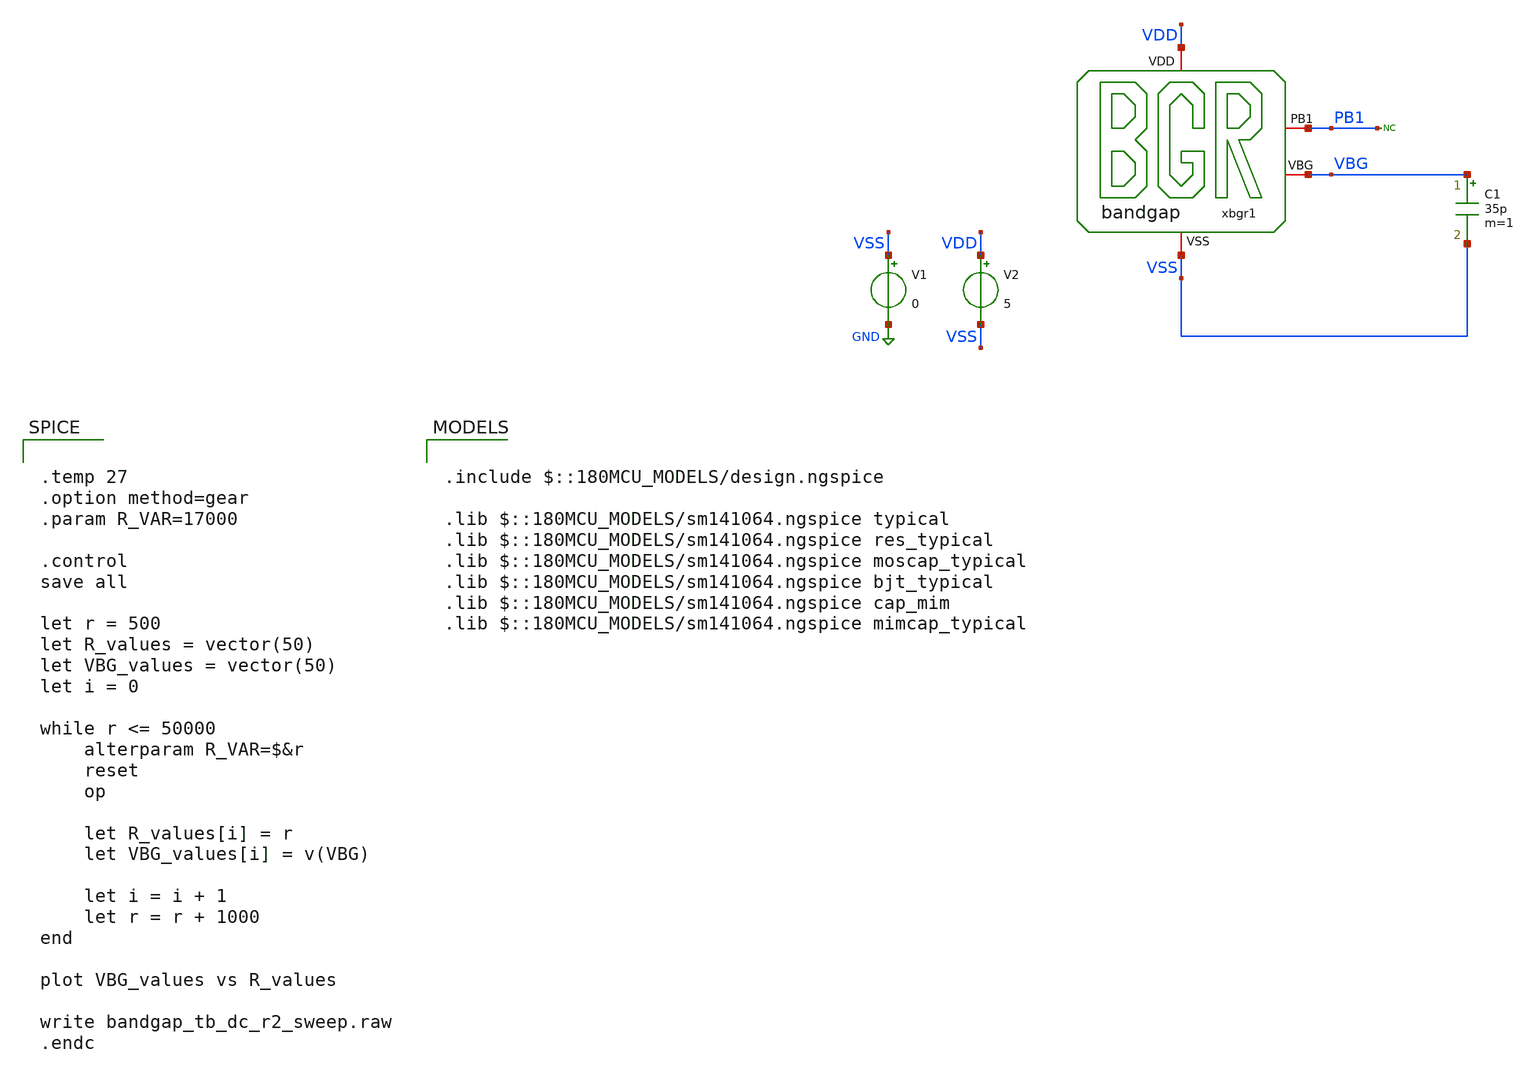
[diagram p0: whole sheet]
** sch_path: bandgap/xschem/sim/bandgap_tb_dc_r2_sweep.sch
**.subckt bandgap_tb_dc_r2_sweep
V1 VSS GND 0
V2 VDD VSS 5
C1 VBG VSS 35p m=1
* noconn PB1
xbgr1 VDD PB1 VBG VSS bandgap
**** begin user architecture code


.temp 27
.option method=gear
.param R_VAR=17000

.control
save all

let r = 500
let R_values = vector(50)
let VBG_values = vector(50)
let i = 0

while r <= 50000
    alterparam R_VAR=$&r
    reset
    op

    let R_values[i] = r
    let VBG_values[i] = v(VBG)

    let i = i + 1
    let r = r + 1000
end

plot VBG_values vs R_values

write bandgap_tb_dc_r2_sweep.raw
.endc



.include $::180MCU_MODELS/design.ngspice

.lib $::180MCU_MODELS/sm141064.ngspice typical
.lib $::180MCU_MODELS/sm141064.ngspice res_typical
.lib $::180MCU_MODELS/sm141064.ngspice moscap_typical
.lib $::180MCU_MODELS/sm141064.ngspice bjt_typical
.lib $::180MCU_MODELS/sm141064.ngspice cap_mim
.lib $::180MCU_MODELS/sm141064.ngspice mimcap_typical

**** end user architecture code
**.ends

* expanding   symbol:  bandgap/xschem/dev/bandgap.sym # of pins=4
** sym_path: bandgap/cace/testbenches/bandgap.sym
** sch_path: bandgap/cace/testbenches/bandgap.sch
.subckt bandgap VDD PB1 VBG VSS
*.iopin VSS
*.iopin VDD
*.iopin PB1
*.iopin VBG
R0 net7 VSET 1.7k m=1
R1 VSET VSS 7.6k m=1
R2 VB0 VBG 17000 m=1
XQ1 PB1 net8 net6 VSS npn_10p00x10p00 m=12
XQ0 VB0 VB0 net3 VSS npn_10p00x10p00 m=1
XM4 VSS net2 VSS VSS nfet_03v3 L=1u W=19u nf=1 ad='int((nf+1)/2) * W/nf * 0.18u' as='int((nf+2)/2) * W/nf * 0.18u'
+ pd='2*int((nf+1)/2) * (W/nf + 0.18u)' ps='2*int((nf+2)/2) * (W/nf + 0.18u)' nrd='0.18u / W' nrs='0.18u / W'
+ sa=0 sb=0 sd=0 m=1
XM2 net2 VSS VDD VDD pfet_03v3 L=10u W=1u nf=1 ad='int((nf+1)/2) * W/nf * 0.18u' as='int((nf+2)/2) * W/nf * 0.18u'
+ pd='2*int((nf+1)/2) * (W/nf + 0.18u)' ps='2*int((nf+2)/2) * (W/nf + 0.18u)' nrd='0.18u / W' nrs='0.18u / W'
+ sa=0 sb=0 sd=0 m=1
XM3 net5 net2 VDD VDD pfet_03v3 L=2u W=2u nf=1 ad='int((nf+1)/2) * W/nf * 0.18u' as='int((nf+2)/2) * W/nf * 0.18u'
+ pd='2*int((nf+1)/2) * (W/nf + 0.18u)' ps='2*int((nf+2)/2) * (W/nf + 0.18u)' nrd='0.18u / W' nrs='0.18u / W'
+ sa=0 sb=0 sd=0 m=1
XM1 net1 net1 VDD VDD pfet_03v3 L=7.4u W=20u nf=1 ad='int((nf+1)/2) * W/nf * 0.18u' as='int((nf+2)/2) * W/nf * 0.18u'
+ pd='2*int((nf+1)/2) * (W/nf + 0.18u)' ps='2*int((nf+2)/2) * (W/nf + 0.18u)' nrd='0.18u / W' nrs='0.18u / W'
+ sa=0 sb=0 sd=0 m=1
XM0 net4 net1 VDD VDD pfet_03v3 L=7.4u W=20u nf=1 ad='int((nf+1)/2) * W/nf * 0.18u' as='int((nf+2)/2) * W/nf * 0.18u'
+ pd='2*int((nf+1)/2) * (W/nf + 0.18u)' ps='2*int((nf+2)/2) * (W/nf + 0.18u)' nrd='0.18u / W' nrs='0.18u / W'
+ sa=0 sb=0 sd=0 m=1
VQ0E net3 VSET 0
VM0D net4 VB0 0
VM3D net5 VB0 0
VQ1E net6 net7 0
VM1D net1 PB1 0
VQ1B VBG net8 0
.ends

.GLOBAL GND
.end
